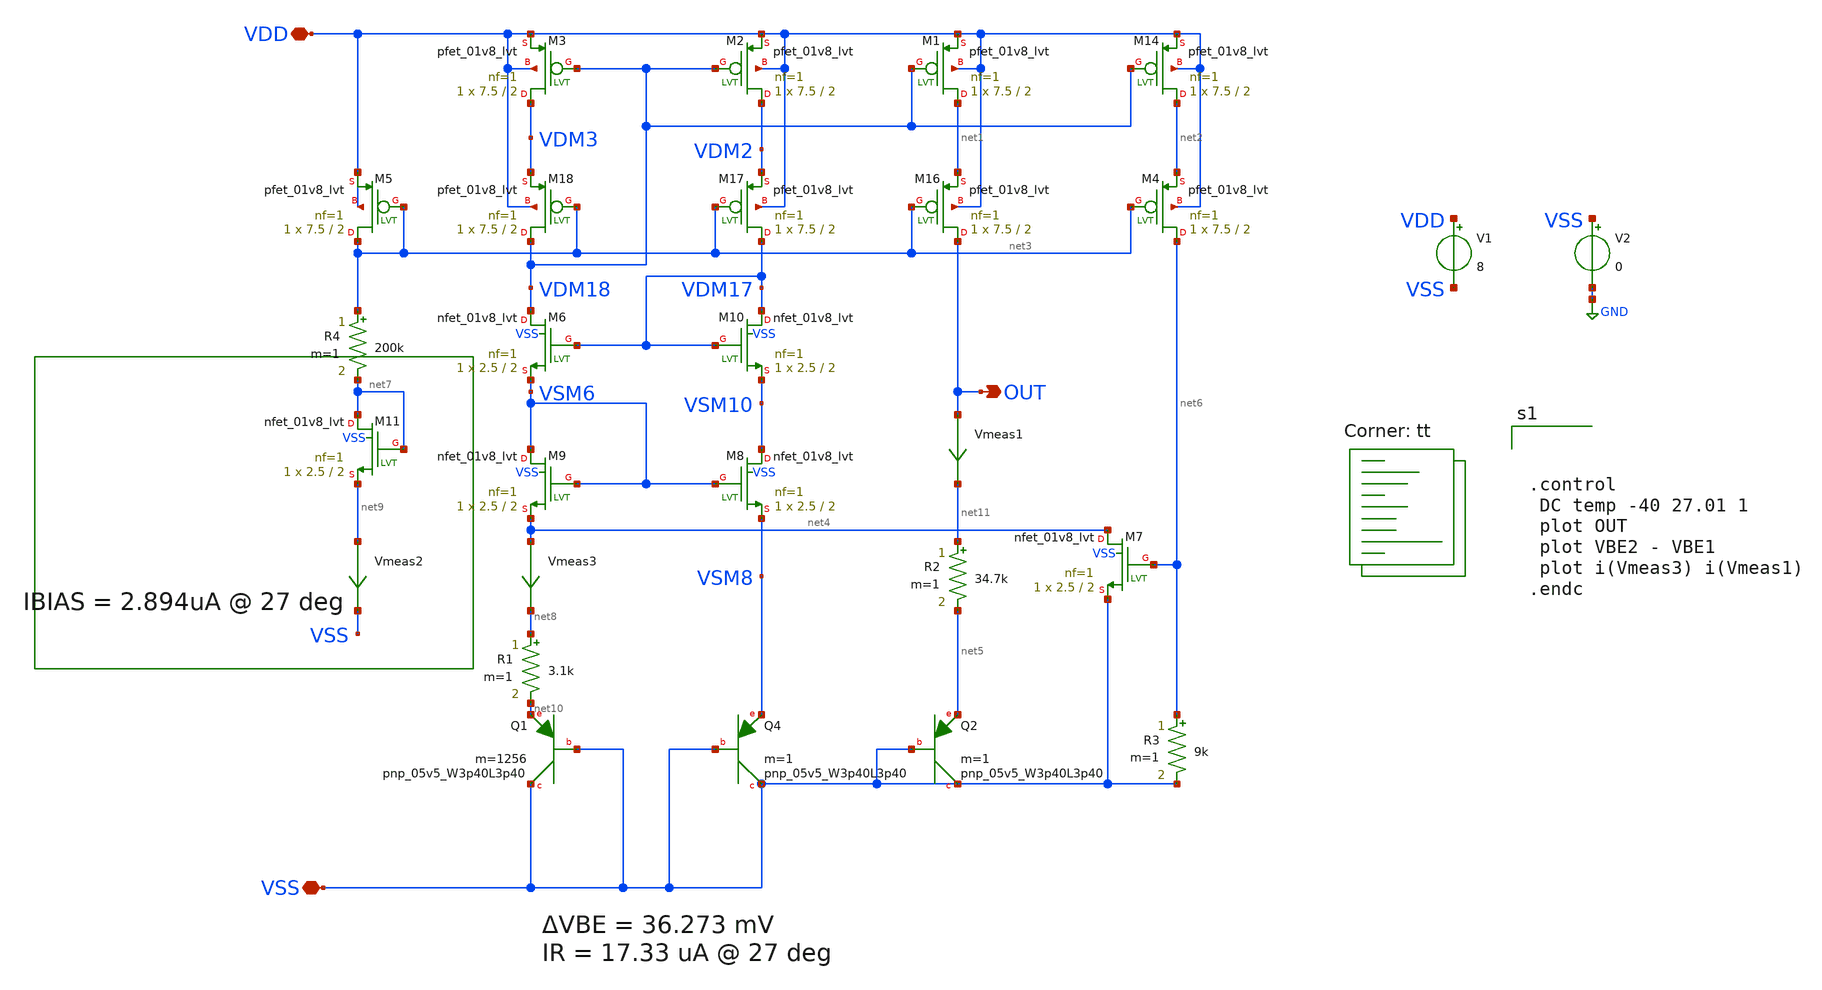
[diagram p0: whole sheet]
** sch_path: bandgap/bgr.sch
**.subckt bgr VDD VSS OUT
*.iopin VDD
*.iopin VSS
*.opin OUT
V1 VDD VSS 8
V2 VSS GND 0
R1 net8 net10 3.1k m=1
R2 net11 net5 34.7k m=1
R3 net6 VSS 9k m=1
XQ4 VSS VSS VSM8 sky130_fd_pr__pnp_05v5_W3p40L3p40 m=1
XQ1 VSS VSS net10 sky130_fd_pr__pnp_05v5_W3p40L3p40 m=1256
XQ2 VSS VSS net5 sky130_fd_pr__pnp_05v5_W3p40L3p40 m=1
XM14 net2 VDM18 VDD VDD sky130_fd_pr__pfet_01v8_lvt L=2 W=7.5 nf=1 ad='int((nf+1)/2) * W/nf * 0.29' as='int((nf+2)/2) * W/nf * 0.29'
+ pd='2*int((nf+1)/2) * (W/nf + 0.29)' ps='2*int((nf+2)/2) * (W/nf + 0.29)' nrd='0.29 / W' nrs='0.29 / W'
+ sa=0 sb=0 sd=0 mult=1 m=1
XM1 net1 VDM18 VDD VDD sky130_fd_pr__pfet_01v8_lvt L=2 W=7.5 nf=1 ad='int((nf+1)/2) * W/nf * 0.29' as='int((nf+2)/2) * W/nf * 0.29'
+ pd='2*int((nf+1)/2) * (W/nf + 0.29)' ps='2*int((nf+2)/2) * (W/nf + 0.29)' nrd='0.29 / W' nrs='0.29 / W'
+ sa=0 sb=0 sd=0 mult=1 m=1
XM2 VDM2 VDM18 VDD VDD sky130_fd_pr__pfet_01v8_lvt L=2 W=7.5 nf=1 ad='int((nf+1)/2) * W/nf * 0.29' as='int((nf+2)/2) * W/nf * 0.29'
+ pd='2*int((nf+1)/2) * (W/nf + 0.29)' ps='2*int((nf+2)/2) * (W/nf + 0.29)' nrd='0.29 / W' nrs='0.29 / W'
+ sa=0 sb=0 sd=0 mult=1 m=1
XM3 VDM3 VDM18 VDD VDD sky130_fd_pr__pfet_01v8_lvt L=2 W=7.5 nf=1 ad='int((nf+1)/2) * W/nf * 0.29' as='int((nf+2)/2) * W/nf * 0.29'
+ pd='2*int((nf+1)/2) * (W/nf + 0.29)' ps='2*int((nf+2)/2) * (W/nf + 0.29)' nrd='0.29 / W' nrs='0.29 / W'
+ sa=0 sb=0 sd=0 mult=1 m=1
XM4 net6 net3 net2 VDD sky130_fd_pr__pfet_01v8_lvt L=2 W=7.5 nf=1 ad='int((nf+1)/2) * W/nf * 0.29' as='int((nf+2)/2) * W/nf * 0.29'
+ pd='2*int((nf+1)/2) * (W/nf + 0.29)' ps='2*int((nf+2)/2) * (W/nf + 0.29)' nrd='0.29 / W' nrs='0.29 / W'
+ sa=0 sb=0 sd=0 mult=1 m=1
XM16 OUT net3 net1 VDD sky130_fd_pr__pfet_01v8_lvt L=2 W=7.5 nf=1 ad='int((nf+1)/2) * W/nf * 0.29' as='int((nf+2)/2) * W/nf * 0.29'
+ pd='2*int((nf+1)/2) * (W/nf + 0.29)' ps='2*int((nf+2)/2) * (W/nf + 0.29)' nrd='0.29 / W' nrs='0.29 / W'
+ sa=0 sb=0 sd=0 mult=1 m=1
XM17 VDM17 net3 VDM2 VDD sky130_fd_pr__pfet_01v8_lvt L=2 W=7.5 nf=1 ad='int((nf+1)/2) * W/nf * 0.29'
+ as='int((nf+2)/2) * W/nf * 0.29' pd='2*int((nf+1)/2) * (W/nf + 0.29)' ps='2*int((nf+2)/2) * (W/nf + 0.29)'
+ nrd='0.29 / W' nrs='0.29 / W' sa=0 sb=0 sd=0 mult=1 m=1
XM18 VDM18 net3 VDM3 VDD sky130_fd_pr__pfet_01v8_lvt L=2 W=7.5 nf=1 ad='int((nf+1)/2) * W/nf * 0.29'
+ as='int((nf+2)/2) * W/nf * 0.29' pd='2*int((nf+1)/2) * (W/nf + 0.29)' ps='2*int((nf+2)/2) * (W/nf + 0.29)'
+ nrd='0.29 / W' nrs='0.29 / W' sa=0 sb=0 sd=0 mult=1 m=1
XM5 net3 net3 VDD VDD sky130_fd_pr__pfet_01v8_lvt L=2 W=7.5 nf=1 ad='int((nf+1)/2) * W/nf * 0.29' as='int((nf+2)/2) * W/nf * 0.29'
+ pd='2*int((nf+1)/2) * (W/nf + 0.29)' ps='2*int((nf+2)/2) * (W/nf + 0.29)' nrd='0.29 / W' nrs='0.29 / W'
+ sa=0 sb=0 sd=0 mult=1 m=1
XM10 VDM17 VDM17 VSM10 VSS sky130_fd_pr__nfet_01v8_lvt L=2 W=2.5 nf=1 ad='int((nf+1)/2) * W/nf * 0.29'
+ as='int((nf+2)/2) * W/nf * 0.29' pd='2*int((nf+1)/2) * (W/nf + 0.29)' ps='2*int((nf+2)/2) * (W/nf + 0.29)'
+ nrd='0.29 / W' nrs='0.29 / W' sa=0 sb=0 sd=0 mult=1 m=1
XM6 VDM18 VDM17 VSM6 VSS sky130_fd_pr__nfet_01v8_lvt L=2 W=2.5 nf=1 ad='int((nf+1)/2) * W/nf * 0.29'
+ as='int((nf+2)/2) * W/nf * 0.29' pd='2*int((nf+1)/2) * (W/nf + 0.29)' ps='2*int((nf+2)/2) * (W/nf + 0.29)'
+ nrd='0.29 / W' nrs='0.29 / W' sa=0 sb=0 sd=0 mult=1 m=1
XM7 net4 net6 VSS VSS sky130_fd_pr__nfet_01v8_lvt L=2 W=2.5 nf=1 ad='int((nf+1)/2) * W/nf * 0.29' as='int((nf+2)/2) * W/nf * 0.29'
+ pd='2*int((nf+1)/2) * (W/nf + 0.29)' ps='2*int((nf+2)/2) * (W/nf + 0.29)' nrd='0.29 / W' nrs='0.29 / W'
+ sa=0 sb=0 sd=0 mult=1 m=1
XM8 VSM10 VSM6 VSM8 VSS sky130_fd_pr__nfet_01v8_lvt L=2 W=2.5 nf=1 ad='int((nf+1)/2) * W/nf * 0.29' as='int((nf+2)/2) * W/nf * 0.29'
+ pd='2*int((nf+1)/2) * (W/nf + 0.29)' ps='2*int((nf+2)/2) * (W/nf + 0.29)' nrd='0.29 / W' nrs='0.29 / W'
+ sa=0 sb=0 sd=0 mult=1 m=1
XM9 VSM6 VSM6 net4 VSS sky130_fd_pr__nfet_01v8_lvt L=2 W=2.5 nf=1 ad='int((nf+1)/2) * W/nf * 0.29' as='int((nf+2)/2) * W/nf * 0.29'
+ pd='2*int((nf+1)/2) * (W/nf + 0.29)' ps='2*int((nf+2)/2) * (W/nf + 0.29)' nrd='0.29 / W' nrs='0.29 / W'
+ sa=0 sb=0 sd=0 mult=1 m=1
R4 net3 net7 200k m=1
XM11 net7 net7 net9 VSS sky130_fd_pr__nfet_01v8_lvt L=2 W=2.5 nf=1 ad='int((nf+1)/2) * W/nf * 0.29' as='int((nf+2)/2) * W/nf * 0.29'
+ pd='2*int((nf+1)/2) * (W/nf + 0.29)' ps='2*int((nf+2)/2) * (W/nf + 0.29)' nrd='0.29 / W' nrs='0.29 / W'
+ sa=0 sb=0 sd=0 mult=1 m=1
Vmeas2 net9 VSS 0
.save i(vmeas2)
Vmeas3 net4 net8 0
.save i(vmeas3)
Vmeas1 OUT net11 0
.save i(vmeas1)
**** begin user architecture code
.lib $::SKYWATER_MODELS/sky130.lib.spice tt



.control
 DC temp -40 27.01 1
 plot OUT
 plot VBE2 - VBE1
 plot i(Vmeas3) i(Vmeas1)
.endc


**** end user architecture code
**.ends
.GLOBAL GND
.end
